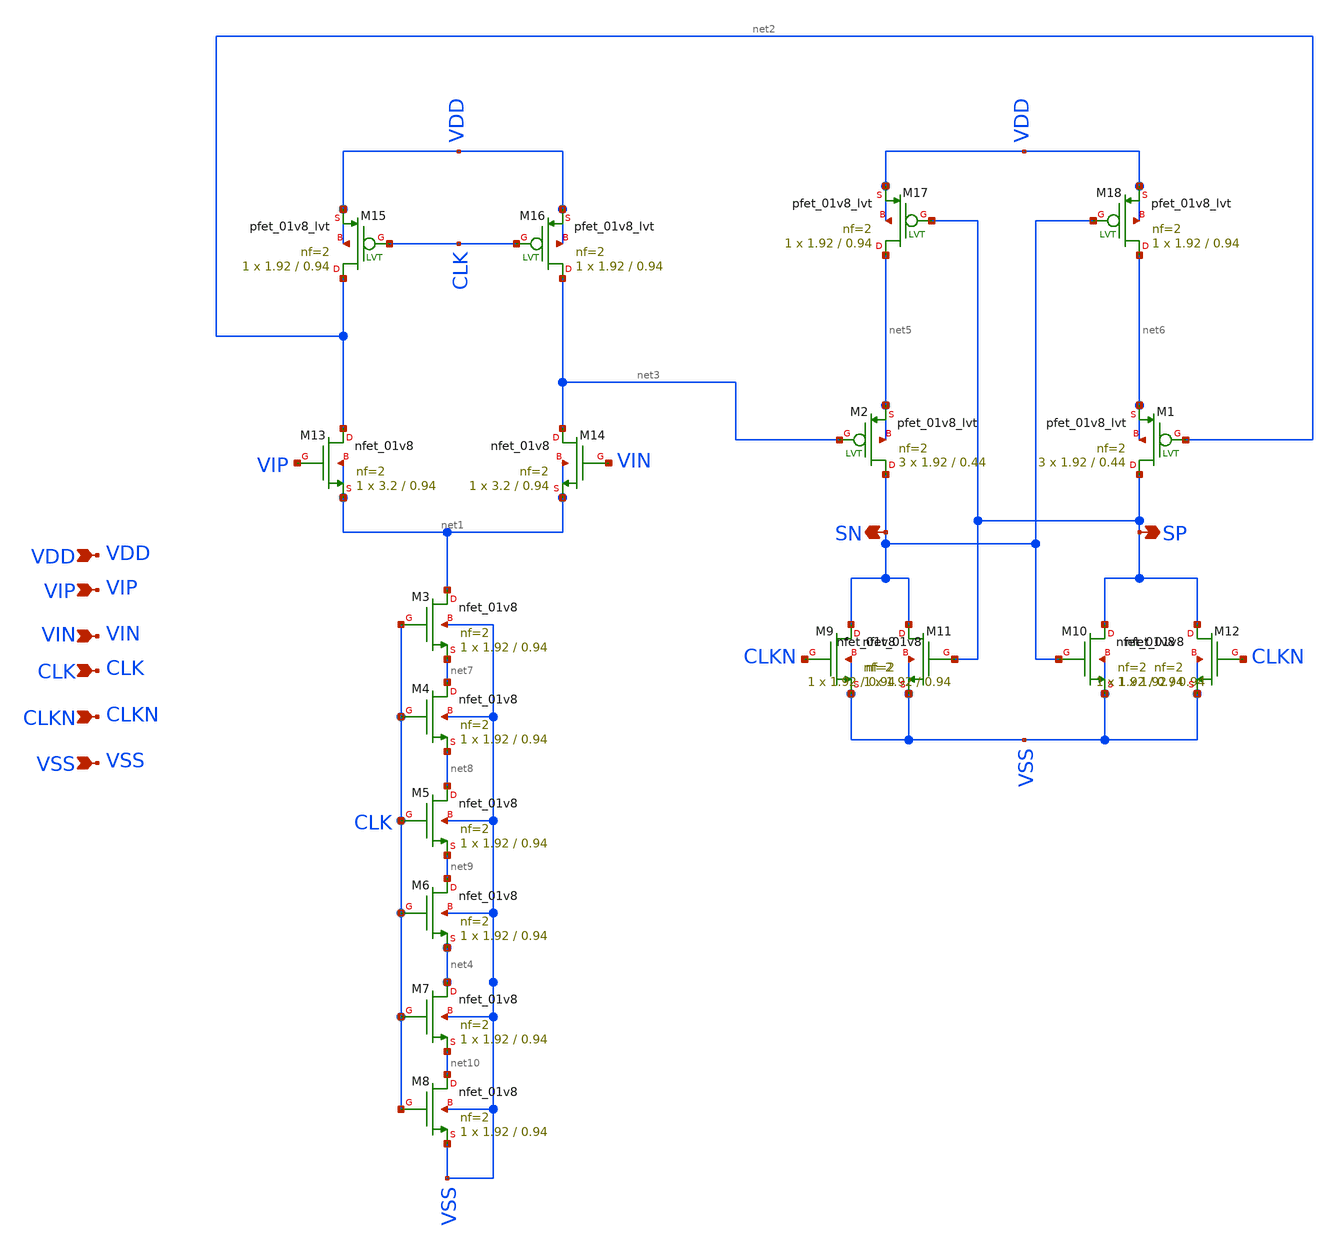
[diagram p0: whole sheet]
** sch_path: design/LELO_SVOD_SKY130A/LELO_CMP2.sch
**.subckt LELO_CMP2 VIP VIN CLK CLKN VDD VSS SN SP
*.ipin VIP
*.ipin VIN
*.ipin CLK
*.ipin CLKN
*.ipin VDD
*.ipin VSS
*.opin SN
*.opin SP
XM2 SN net3 net5 net5 sky130_fd_pr__pfet_01v8_lvt L=0.44 W=1.92 nf=2 ad='int((2 + 1)/2) * 1.92 / 2 * 0.29'
+ as='int((2 + 2)/2) * 1.92 / 2 * 0.29' pd='2*int((2 + 1)/2) * (1.92 / 2 + 0.29)' ps='2*int((2 + 2)/2) * (1.92 / 2 + 0.29)'
+ nrd='0.29 / 1.92 ' nrs='0.29 / 1.92 ' sa=0 sb=0 sd=0 mult=3 m=3
XM1 SP net2 net6 net6 sky130_fd_pr__pfet_01v8_lvt L=0.44 W=1.92 nf=2 ad='int((2 + 1)/2) * 1.92 / 2 * 0.29'
+ as='int((2 + 2)/2) * 1.92 / 2 * 0.29' pd='2*int((2 + 1)/2) * (1.92 / 2 + 0.29)' ps='2*int((2 + 2)/2) * (1.92 / 2 + 0.29)'
+ nrd='0.29 / 1.92 ' nrs='0.29 / 1.92 ' sa=0 sb=0 sd=0 mult=3 m=3
XM3 net1 CLK net7 VSS sky130_fd_pr__nfet_01v8 L=0.94 W=1.92 nf=2 ad='int((2 + 1)/2) * 1.92 / 2 * 0.29'
+ as='int((2 + 2)/2) * 1.92 / 2 * 0.29' pd='2*int((2 + 1)/2) * (1.92 / 2 + 0.29)' ps='2*int((2 + 2)/2) * (1.92 / 2 + 0.29)'
+ nrd='0.29 / 1.92 ' nrs='0.29 / 1.92 ' sa=0 sb=0 sd=0 mult=1 m=1
XM4 net7 CLK net8 VSS sky130_fd_pr__nfet_01v8 L=0.94 W=1.92 nf=2 ad='int((2 + 1)/2) * 1.92 / 2 * 0.29'
+ as='int((2 + 2)/2) * 1.92 / 2 * 0.29' pd='2*int((2 + 1)/2) * (1.92 / 2 + 0.29)' ps='2*int((2 + 2)/2) * (1.92 / 2 + 0.29)'
+ nrd='0.29 / 1.92 ' nrs='0.29 / 1.92 ' sa=0 sb=0 sd=0 mult=1 m=1
XM5 net8 CLK net9 VSS sky130_fd_pr__nfet_01v8 L=0.94 W=1.92 nf=2 ad='int((2 + 1)/2) * 1.92 / 2 * 0.29'
+ as='int((2 + 2)/2) * 1.92 / 2 * 0.29' pd='2*int((2 + 1)/2) * (1.92 / 2 + 0.29)' ps='2*int((2 + 2)/2) * (1.92 / 2 + 0.29)'
+ nrd='0.29 / 1.92 ' nrs='0.29 / 1.92 ' sa=0 sb=0 sd=0 mult=1 m=1
XM6 net9 CLK net4 VSS sky130_fd_pr__nfet_01v8 L=0.94 W=1.92 nf=2 ad='int((2 + 1)/2) * 1.92 / 2 * 0.29'
+ as='int((2 + 2)/2) * 1.92 / 2 * 0.29' pd='2*int((2 + 1)/2) * (1.92 / 2 + 0.29)' ps='2*int((2 + 2)/2) * (1.92 / 2 + 0.29)'
+ nrd='0.29 / 1.92 ' nrs='0.29 / 1.92 ' sa=0 sb=0 sd=0 mult=1 m=1
XM7 net4 CLK net10 VSS sky130_fd_pr__nfet_01v8 L=0.94 W=1.92 nf=2 ad='int((2 + 1)/2) * 1.92 / 2 * 0.29'
+ as='int((2 + 2)/2) * 1.92 / 2 * 0.29' pd='2*int((2 + 1)/2) * (1.92 / 2 + 0.29)' ps='2*int((2 + 2)/2) * (1.92 / 2 + 0.29)'
+ nrd='0.29 / 1.92 ' nrs='0.29 / 1.92 ' sa=0 sb=0 sd=0 mult=1 m=1
XM8 net10 CLK VSS VSS sky130_fd_pr__nfet_01v8 L=0.94 W=1.92 nf=2 ad='int((2 + 1)/2) * 1.92 / 2 * 0.29'
+ as='int((2 + 2)/2) * 1.92 / 2 * 0.29' pd='2*int((2 + 1)/2) * (1.92 / 2 + 0.29)' ps='2*int((2 + 2)/2) * (1.92 / 2 + 0.29)'
+ nrd='0.29 / 1.92 ' nrs='0.29 / 1.92 ' sa=0 sb=0 sd=0 mult=1 m=1
XM9 SN CLKN VSS VSS sky130_fd_pr__nfet_01v8 L=0.94 W=1.92 nf=2 ad='int((2 + 1)/2) * 1.92 / 2 * 0.29'
+ as='int((2 + 2)/2) * 1.92 / 2 * 0.29' pd='2*int((2 + 1)/2) * (1.92 / 2 + 0.29)' ps='2*int((2 + 2)/2) * (1.92 / 2 + 0.29)'
+ nrd='0.29 / 1.92 ' nrs='0.29 / 1.92 ' sa=0 sb=0 sd=0 mult=1 m=1
XM10 SP SN VSS VSS sky130_fd_pr__nfet_01v8 L=0.94 W=1.92 nf=2 ad='int((2 + 1)/2) * 1.92 / 2 * 0.29' as='int((2 + 2)/2) * 1.92 / 2 * 0.29'
+ pd='2*int((2 + 1)/2) * (1.92 / 2 + 0.29)' ps='2*int((2 + 2)/2) * (1.92 / 2 + 0.29)' nrd='0.29 / 1.92 '
+ nrs='0.29 / 1.92 ' sa=0 sb=0 sd=0 mult=1 m=1
XM11 SN SP VSS VSS sky130_fd_pr__nfet_01v8 L=0.94 W=1.92 nf=2 ad='int((2 + 1)/2) * 1.92 / 2 * 0.29' as='int((2 + 2)/2) * 1.92 / 2 * 0.29'
+ pd='2*int((2 + 1)/2) * (1.92 / 2 + 0.29)' ps='2*int((2 + 2)/2) * (1.92 / 2 + 0.29)' nrd='0.29 / 1.92 '
+ nrs='0.29 / 1.92 ' sa=0 sb=0 sd=0 mult=1 m=1
XM12 SP CLKN VSS VSS sky130_fd_pr__nfet_01v8 L=0.94 W=1.92 nf=2 ad='int((2 + 1)/2) * 1.92 / 2 * 0.29'
+ as='int((2 + 2)/2) * 1.92 / 2 * 0.29' pd='2*int((2 + 1)/2) * (1.92 / 2 + 0.29)' ps='2*int((2 + 2)/2) * (1.92 / 2 + 0.29)'
+ nrd='0.29 / 1.92 ' nrs='0.29 / 1.92 ' sa=0 sb=0 sd=0 mult=1 m=1
XM13 net2 VIP net1 net1 sky130_fd_pr__nfet_01v8 L=0.94 W=3.2 nf=2 ad='int((2 + 1)/2) * 3.2 / 2 * 0.29'
+ as='int((2 + 2)/2) * 3.2 / 2 * 0.29' pd='2*int((2 + 1)/2) * (3.2 / 2 + 0.29)' ps='2*int((2 + 2)/2) * (3.2 / 2 + 0.29)'
+ nrd='0.29 / 3.2 ' nrs='0.29 / 3.2 ' sa=0 sb=0 sd=0 mult=1 m=1
XM14 net3 VIN net1 net1 sky130_fd_pr__nfet_01v8 L=0.94 W=3.2 nf=2 ad='int((2 + 1)/2) * 3.2 / 2 * 0.29'
+ as='int((2 + 2)/2) * 3.2 / 2 * 0.29' pd='2*int((2 + 1)/2) * (3.2 / 2 + 0.29)' ps='2*int((2 + 2)/2) * (3.2 / 2 + 0.29)'
+ nrd='0.29 / 3.2 ' nrs='0.29 / 3.2 ' sa=0 sb=0 sd=0 mult=1 m=1
XM15 net2 CLK VDD VDD sky130_fd_pr__pfet_01v8_lvt L=0.94 W=1.92 nf=2 ad='int((2 + 1)/2) * 1.92 / 2 * 0.29'
+ as='int((2 + 2)/2) * 1.92 / 2 * 0.29' pd='2*int((2 + 1)/2) * (1.92 / 2 + 0.29)' ps='2*int((2 + 2)/2) * (1.92 / 2 + 0.29)'
+ nrd='0.29 / 1.92 ' nrs='0.29 / 1.92 ' sa=0 sb=0 sd=0 mult=1 m=1
XM16 net3 CLK VDD VDD sky130_fd_pr__pfet_01v8_lvt L=0.94 W=1.92 nf=2 ad='int((2 + 1)/2) * 1.92 / 2 * 0.29'
+ as='int((2 + 2)/2) * 1.92 / 2 * 0.29' pd='2*int((2 + 1)/2) * (1.92 / 2 + 0.29)' ps='2*int((2 + 2)/2) * (1.92 / 2 + 0.29)'
+ nrd='0.29 / 1.92 ' nrs='0.29 / 1.92 ' sa=0 sb=0 sd=0 mult=1 m=1
XM17 net5 SP VDD VDD sky130_fd_pr__pfet_01v8_lvt L=0.94 W=1.92 nf=2 ad='int((2 + 1)/2) * 1.92 / 2 * 0.29'
+ as='int((2 + 2)/2) * 1.92 / 2 * 0.29' pd='2*int((2 + 1)/2) * (1.92 / 2 + 0.29)' ps='2*int((2 + 2)/2) * (1.92 / 2 + 0.29)'
+ nrd='0.29 / 1.92 ' nrs='0.29 / 1.92 ' sa=0 sb=0 sd=0 mult=1 m=1
XM18 net6 SN VDD VDD sky130_fd_pr__pfet_01v8_lvt L=0.94 W=1.92 nf=2 ad='int((2 + 1)/2) * 1.92 / 2 * 0.29'
+ as='int((2 + 2)/2) * 1.92 / 2 * 0.29' pd='2*int((2 + 1)/2) * (1.92 / 2 + 0.29)' ps='2*int((2 + 2)/2) * (1.92 / 2 + 0.29)'
+ nrd='0.29 / 1.92 ' nrs='0.29 / 1.92 ' sa=0 sb=0 sd=0 mult=1 m=1
**.ends
.end
